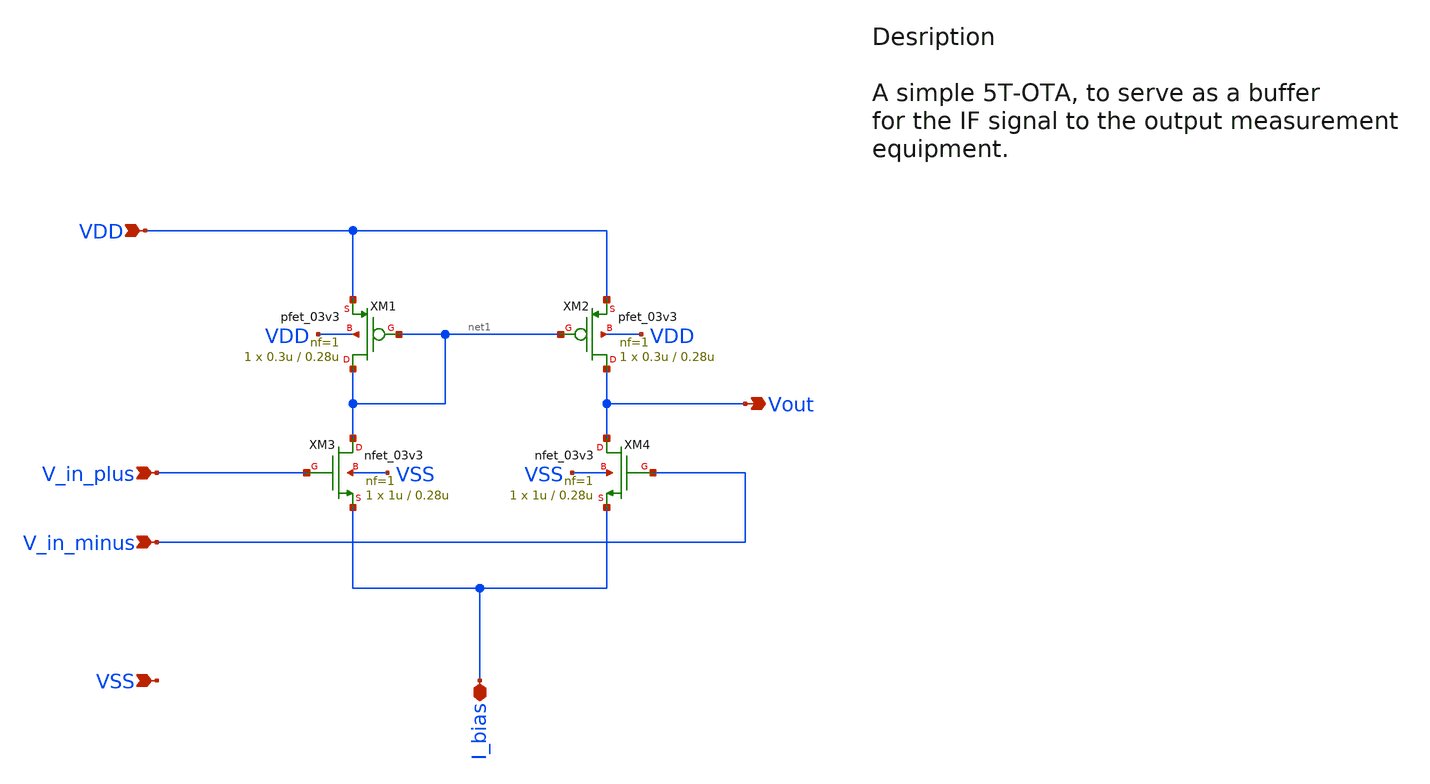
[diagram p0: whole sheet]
** sch_path: designs/libs/core_top/A5_Time_Transcenders/schematics/5T-OTA-buffer_no_hierarchy.sch
**.subckt 5T-OTA-buffer_no_hierarchy VDD V_in_plus V_in_minus Vout I_bias VSS
*.ipin VDD
*.ipin V_in_plus
*.ipin V_in_minus
*.opin Vout
*.iopin I_bias
*.ipin VSS
XM3 net1 V_in_plus I_bias VSS nfet_03v3 L=0.28u W=1u nf=1 ad='int((nf+1)/2) * W/nf * 0.18u' as='int((nf+2)/2) * W/nf * 0.18u'
+ pd='2*int((nf+1)/2) * (W/nf + 0.18u)' ps='2*int((nf+2)/2) * (W/nf + 0.18u)' nrd='0.18u / W' nrs='0.18u / W'
+ sa=0 sb=0 sd=0 m=1
XM4 Vout V_in_minus I_bias VSS nfet_03v3 L=0.28u W=1u nf=1 ad='int((nf+1)/2) * W/nf * 0.18u' as='int((nf+2)/2) * W/nf * 0.18u'
+ pd='2*int((nf+1)/2) * (W/nf + 0.18u)' ps='2*int((nf+2)/2) * (W/nf + 0.18u)' nrd='0.18u / W' nrs='0.18u / W'
+ sa=0 sb=0 sd=0 m=1
XM1 net1 net1 VDD VDD pfet_03v3 L=0.28u W=0.3u nf=1 ad='int((nf+1)/2) * W/nf * 0.18u' as='int((nf+2)/2) * W/nf * 0.18u'
+ pd='2*int((nf+1)/2) * (W/nf + 0.18u)' ps='2*int((nf+2)/2) * (W/nf + 0.18u)' nrd='0.18u / W' nrs='0.18u / W'
+ sa=0 sb=0 sd=0 m=1
XM2 Vout net1 VDD VDD pfet_03v3 L=0.28u W=0.3u nf=1 ad='int((nf+1)/2) * W/nf * 0.18u' as='int((nf+2)/2) * W/nf * 0.18u'
+ pd='2*int((nf+1)/2) * (W/nf + 0.18u)' ps='2*int((nf+2)/2) * (W/nf + 0.18u)' nrd='0.18u / W' nrs='0.18u / W'
+ sa=0 sb=0 sd=0 m=1
**** begin user architecture code

.include $::180MCU_MODELS/design.ngspice
.lib $::180MCU_MODELS/sm141064.ngspice typical
.lib $::180MCU_MODELS/sm141064.ngspice mimcap_typical
.lib $::180MCU_MODELS/sm141064.ngspice cap_mim
.lib $::180MCU_MODELS/sm141064.ngspice res_typical


**** end user architecture code
**.ends
.end
